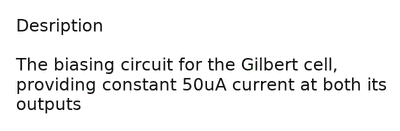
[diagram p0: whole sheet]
** sch_path: src/design_xsch/Biasing_network_no_hierarchy.sch
**.subckt Biasing_network_no_hierarchy
**** begin user architecture code

.include $::180MCU_MODELS/design.ngspice
.lib $::180MCU_MODELS/sm141064.ngspice typical
.lib $::180MCU_MODELS/sm141064.ngspice mimcap_typical
.lib $::180MCU_MODELS/sm141064.ngspice cap_mim
.lib $::180MCU_MODELS/sm141064.ngspice res_typical




* let sets vectors to a plot, while set sets a variable, globally accessible in .control
.control

    * Set frequency and amplitude variables to proper values from within the control sequence
    save all

    op
    show

    write Biasing_network_sim.raw

    set appendwrite

    * Transient analysis to observe mixing operation
    tran 1p 10n


    write Biasing_network_sim.raw

.endc


**** end user architecture code
**.ends
.end
